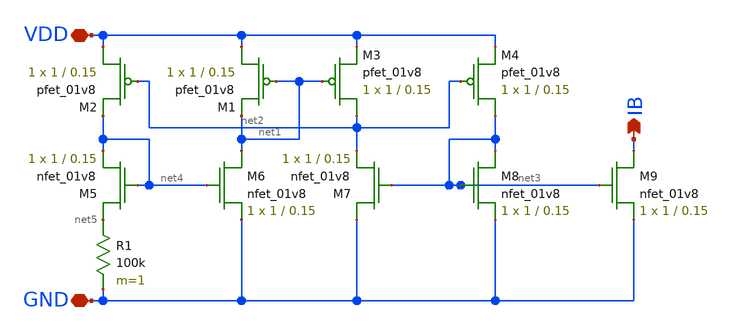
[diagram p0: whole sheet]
** sch_path: schematics/bias_generator.sch
**.subckt bias_generator VDD GND IB
*.iopin VDD
*.iopin GND
*.opin IB
XM2 VDD net2 net4 VDD sky130_fd_pr__pfet_01v8 L=0.15 W=1 nf=1 ad='int((nf+1)/2) * W/nf * 0.29' as='int((nf+2)/2) * W/nf * 0.29'
+ pd='2*int((nf+1)/2) * (W/nf + 0.29)' ps='2*int((nf+2)/2) * (W/nf + 0.29)' nrd='0.29 / W' nrs='0.29 / W'
+ sa=0 sb=0 sd=0 mult=1 m=1
XM1 VDD net1 net1 VDD sky130_fd_pr__pfet_01v8 L=0.15 W=1 nf=1 ad='int((nf+1)/2) * W/nf * 0.29' as='int((nf+2)/2) * W/nf * 0.29'
+ pd='2*int((nf+1)/2) * (W/nf + 0.29)' ps='2*int((nf+2)/2) * (W/nf + 0.29)' nrd='0.29 / W' nrs='0.29 / W'
+ sa=0 sb=0 sd=0 mult=1 m=1
XM3 net2 net1 VDD VDD sky130_fd_pr__pfet_01v8 L=0.15 W=1 nf=1 ad='int((nf+1)/2) * W/nf * 0.29' as='int((nf+2)/2) * W/nf * 0.29'
+ pd='2*int((nf+1)/2) * (W/nf + 0.29)' ps='2*int((nf+2)/2) * (W/nf + 0.29)' nrd='0.29 / W' nrs='0.29 / W'
+ sa=0 sb=0 sd=0 mult=1 m=1
XM4 net3 net2 VDD VDD sky130_fd_pr__pfet_01v8 L=0.15 W=1 nf=1 ad='int((nf+1)/2) * W/nf * 0.29' as='int((nf+2)/2) * W/nf * 0.29'
+ pd='2*int((nf+1)/2) * (W/nf + 0.29)' ps='2*int((nf+2)/2) * (W/nf + 0.29)' nrd='0.29 / W' nrs='0.29 / W'
+ sa=0 sb=0 sd=0 mult=1 m=1
XM5 net5 net4 net4 GND sky130_fd_pr__nfet_01v8 L=0.15 W=1 nf=1 ad='int((nf+1)/2) * W/nf * 0.29' as='int((nf+2)/2) * W/nf * 0.29'
+ pd='2*int((nf+1)/2) * (W/nf + 0.29)' ps='2*int((nf+2)/2) * (W/nf + 0.29)' nrd='0.29 / W' nrs='0.29 / W'
+ sa=0 sb=0 sd=0 mult=1 m=1
XM6 net1 net4 GND GND sky130_fd_pr__nfet_01v8 L=0.15 W=1 nf=1 ad='int((nf+1)/2) * W/nf * 0.29' as='int((nf+2)/2) * W/nf * 0.29'
+ pd='2*int((nf+1)/2) * (W/nf + 0.29)' ps='2*int((nf+2)/2) * (W/nf + 0.29)' nrd='0.29 / W' nrs='0.29 / W'
+ sa=0 sb=0 sd=0 mult=1 m=1
XM7 GND net3 net2 GND sky130_fd_pr__nfet_01v8 L=0.15 W=1 nf=1 ad='int((nf+1)/2) * W/nf * 0.29' as='int((nf+2)/2) * W/nf * 0.29'
+ pd='2*int((nf+1)/2) * (W/nf + 0.29)' ps='2*int((nf+2)/2) * (W/nf + 0.29)' nrd='0.29 / W' nrs='0.29 / W'
+ sa=0 sb=0 sd=0 mult=1 m=1
XM8 net3 net3 GND GND sky130_fd_pr__nfet_01v8 L=0.15 W=1 nf=1 ad='int((nf+1)/2) * W/nf * 0.29' as='int((nf+2)/2) * W/nf * 0.29'
+ pd='2*int((nf+1)/2) * (W/nf + 0.29)' ps='2*int((nf+2)/2) * (W/nf + 0.29)' nrd='0.29 / W' nrs='0.29 / W'
+ sa=0 sb=0 sd=0 mult=1 m=1
R1 net5 GND 100k m=1
XM9 IB net3 GND GND sky130_fd_pr__nfet_01v8 L=0.15 W=1 nf=1 ad='int((nf+1)/2) * W/nf * 0.29' as='int((nf+2)/2) * W/nf * 0.29'
+ pd='2*int((nf+1)/2) * (W/nf + 0.29)' ps='2*int((nf+2)/2) * (W/nf + 0.29)' nrd='0.29 / W' nrs='0.29 / W'
+ sa=0 sb=0 sd=0 mult=1 m=1
**.ends
.end
